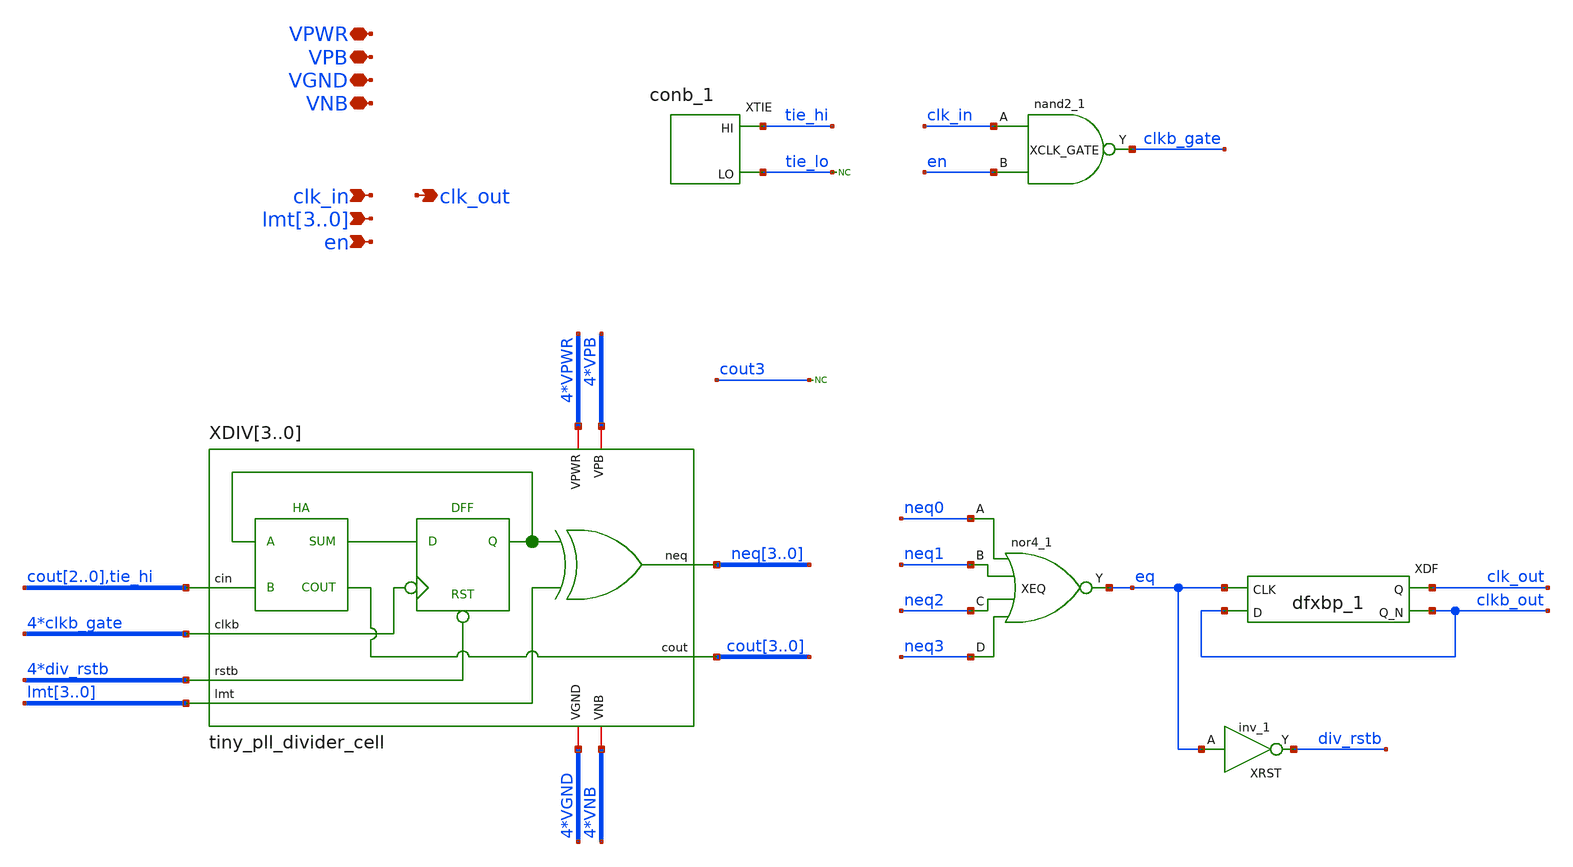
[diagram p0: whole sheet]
** sch_path: xschem/tiny_pll/tiny_pll_divider.sch
**.subckt tiny_pll_divider clk_in lmt3,lmt2,lmt1,lmt0 clk_out VPWR VPB VGND VNB en
*.ipin clk_in
*.ipin lmt3,lmt2,lmt1,lmt0
*.opin clk_out
*.iopin VPWR
*.iopin VPB
*.iopin VGND
*.iopin VNB
*.ipin en
XDIV3 VPWR VPB VGND VNB clkb_gate cout3 cout2 neq3 lmt3 div_rstb tiny_pll_divider_cell
XDIV2 VPWR VPB VGND VNB clkb_gate cout2 cout1 neq2 lmt2 div_rstb tiny_pll_divider_cell
XDIV1 VPWR VPB VGND VNB clkb_gate cout1 cout0 neq1 lmt1 div_rstb tiny_pll_divider_cell
XDIV0 VPWR VPB VGND VNB clkb_gate cout0 tie_hi neq0 lmt0 div_rstb tiny_pll_divider_cell
XEQ neq0 neq1 neq2 neq3 VGND VNB VPB VPWR eq sky130_fd_sc_hd__nor4_1
* noconn cout3
XRST eq VGND VNB VPB VPWR div_rstb sky130_fd_sc_hd__inv_1
XDF eq clkb_out VGND VNB VPB VPWR clk_out clkb_out sky130_fd_sc_hd__dfxbp_1
XCLK_GATE clk_in en VGND VNB VPB VPWR clkb_gate sky130_fd_sc_hd__nand2_1
XTIE VGND VNB VPB VPWR tie_hi tie_lo sky130_fd_sc_hd__conb_1
* noconn tie_lo
**.ends

* expanding   symbol:  tiny_pll_divider_cell.sym # of pins=10
** sym_path: xschem/tiny_pll/tiny_pll_divider_cell.sym
** sch_path: xschem/tiny_pll/tiny_pll_divider_cell.sch
.subckt tiny_pll_divider_cell VPWR VPB VGND VNB clkb cout cin neq lmt rstb
*.ipin cin
*.ipin lmt
*.ipin clkb
*.opin cout
*.opin neq
*.iopin VPWR
*.iopin VPB
*.iopin VGND
*.iopin VNB
*.ipin rstb
XHA dout cin VGND VNB VPB VPWR cout sum sky130_fd_sc_hd__ha_1
XEQ lmt dout VGND VNB VPB VPWR neq sky130_fd_sc_hd__xor2_1
XDF clkb sum rstb VGND VNB VPB VPWR dout sky130_fd_sc_hd__dfrtn_1
.ends

.end
